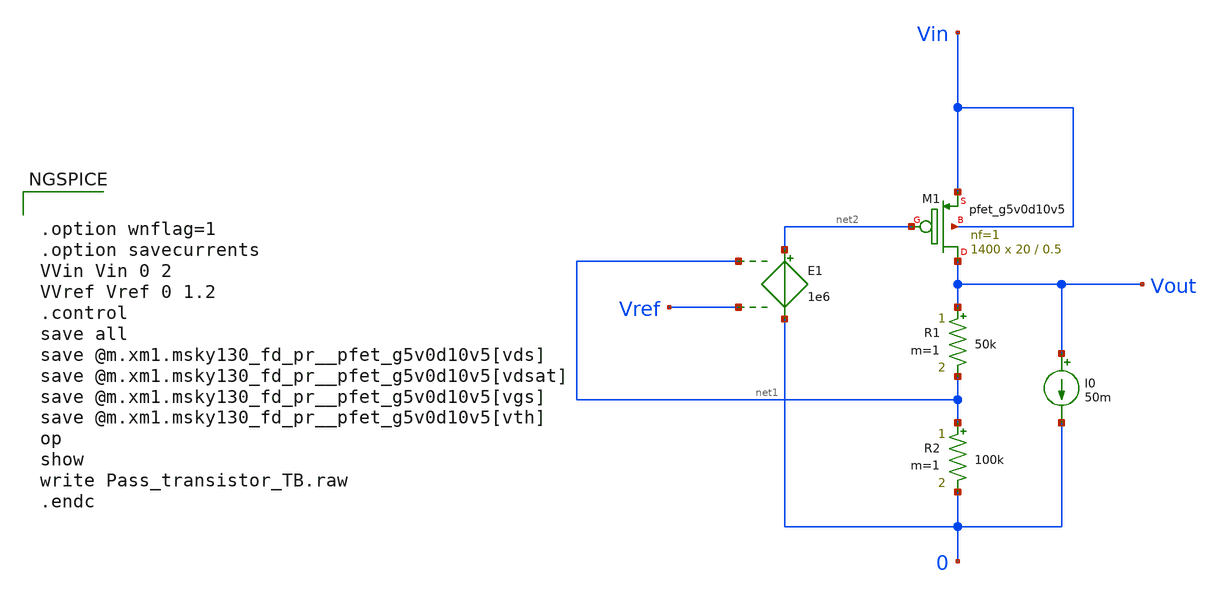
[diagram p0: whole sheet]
** sch_path: Analog_Blocks/LDO/Testbench/Pass_transistor_TB.sch
**.subckt Pass_transistor_TB
XM1 Vout net2 Vin Vin sky130_fd_pr__pfet_g5v0d10v5 L=0.5 W=20 nf=1 ad='int((nf+1)/2) * W/nf * 0.29' as='int((nf+2)/2) * W/nf * 0.29'
+ pd='2*int((nf+1)/2) * (W/nf + 0.29)' ps='2*int((nf+2)/2) * (W/nf + 0.29)' nrd='0.29 / W' nrs='0.29 / W'
+ sa=0 sb=0 sd=0 mult=1400 m=1400
R1 Vout net1 50k m=1
R2 net1 0 100k m=1
E1 net2 0 net1 Vref 1e6
I0 Vout 0 50m
**** begin user architecture code


.option wnflag=1
.option savecurrents
VVin Vin 0 2
VVref Vref 0 1.2
.control
save all
save @m.xm1.msky130_fd_pr__pfet_g5v0d10v5[vds]
save @m.xm1.msky130_fd_pr__pfet_g5v0d10v5[vdsat]
save @m.xm1.msky130_fd_pr__pfet_g5v0d10v5[vgs]
save @m.xm1.msky130_fd_pr__pfet_g5v0d10v5[vth]
op
show
write Pass_transistor_TB.raw
.endc




.param mc_mm_switch=0
.param mc_pr_switch=0
.include ~/mabrains/Analog_blocks/models/sky130A/libs.ref/sky130_fd_pr/spice/sky130_fd_pr__nfet_01v8__sf.corner.spice
.include ~/mabrains/Analog_blocks/models/sky130A/libs.ref/sky130_fd_pr/spice/sky130_fd_pr__nfet_01v8_lvt__sf.corner.spice
.include ~/mabrains/Analog_blocks/models/sky130A/libs.ref/sky130_fd_pr/spice/sky130_fd_pr__pfet_01v8__sf.corner.spice
.include ~/mabrains/Analog_blocks/models/sky130A/libs.ref/sky130_fd_pr/spice/sky130_fd_pr__nfet_03v3_nvt__sf.corner.spice
.include ~/mabrains/Analog_blocks/models/sky130A/libs.ref/sky130_fd_pr/spice/sky130_fd_pr__nfet_05v0_nvt__sf.corner.spice
.include ~/mabrains/Analog_blocks/models/sky130A/libs.ref/sky130_fd_pr/spice/sky130_fd_pr__esd_nfet_01v8__sf.corner.spice
.include ~/mabrains/Analog_blocks/models/sky130A/libs.ref/sky130_fd_pr/spice/sky130_fd_pr__pfet_01v8_lvt__sf.corner.spice
.include ~/mabrains/Analog_blocks/models/sky130A/libs.ref/sky130_fd_pr/spice/sky130_fd_pr__pfet_01v8_hvt__sf.corner.spice
.include ~/mabrains/Analog_blocks/models/sky130A/libs.ref/sky130_fd_pr/spice/sky130_fd_pr__esd_pfet_g5v0d10v5__sf.corner.spice
.include ~/mabrains/Analog_blocks/models/sky130A/libs.ref/sky130_fd_pr/spice/sky130_fd_pr__pfet_g5v0d10v5__sf.corner.spice
.include ~/mabrains/Analog_blocks/models/sky130A/libs.ref/sky130_fd_pr/spice/sky130_fd_pr__pfet_g5v0d16v0__sf.corner.spice
.include ~/mabrains/Analog_blocks/models/sky130A/libs.ref/sky130_fd_pr/spice/sky130_fd_pr__nfet_g5v0d10v5__sf.corner.spice
.include ~/mabrains/Analog_blocks/models/sky130A/libs.ref/sky130_fd_pr/spice/sky130_fd_pr__nfet_g5v0d16v0__sf_discrete.corner.spice
.include ~/mabrains/Analog_blocks/models/sky130A/libs.ref/sky130_fd_pr/spice/sky130_fd_pr__esd_nfet_g5v0d10v5__sf.corner.spice
.include ~/mabrains/Analog_blocks/models/sky130A/libs.ref/sky130_fd_pr/spice/sky130_fd_pr__pfet_20v0__sf_discrete.corner.spice
.include ~/mabrains/Analog_blocks/models/sky130A/libs.ref/sky130_fd_pr/spice/sky130_fd_pr__nfet_20v0__sf_discrete.corner.spice
.include ~/mabrains/Analog_blocks/models/sky130A/libs.tech/ngspice/corners/sf/nonfet.spice
* Mismatch parameters
.include ~/mabrains/Analog_blocks/models/sky130A/libs.ref/sky130_fd_pr/spice/sky130_fd_pr__nfet_01v8__mismatch.corner.spice
.include ~/mabrains/Analog_blocks/models/sky130A/libs.ref/sky130_fd_pr/spice/sky130_fd_pr__pfet_01v8__mismatch.corner.spice
.include ~/mabrains/Analog_blocks/models/sky130A/libs.ref/sky130_fd_pr/spice/sky130_fd_pr__nfet_01v8_lvt__mismatch.corner.spice
.include ~/mabrains/Analog_blocks/models/sky130A/libs.ref/sky130_fd_pr/spice/sky130_fd_pr__pfet_01v8_lvt__mismatch.corner.spice
.include ~/mabrains/Analog_blocks/models/sky130A/libs.ref/sky130_fd_pr/spice/sky130_fd_pr__pfet_01v8_hvt__mismatch.corner.spice
.include ~/mabrains/Analog_blocks/models/sky130A/libs.ref/sky130_fd_pr/spice/sky130_fd_pr__nfet_g5v0d10v5__mismatch.corner.spice
.include ~/mabrains/Analog_blocks/models/sky130A/libs.ref/sky130_fd_pr/spice/sky130_fd_pr__pfet_g5v0d10v5__mismatch.corner.spice
.include ~/mabrains/Analog_blocks/models/sky130A/libs.ref/sky130_fd_pr/spice/sky130_fd_pr__nfet_05v0_nvt__mismatch.corner.spice
.include ~/mabrains/Analog_blocks/models/sky130A/libs.ref/sky130_fd_pr/spice/sky130_fd_pr__nfet_03v3_nvt__mismatch.corner.spice
* Resistor/Capacitor
.include ~/mabrains/Analog_blocks/models/sky130A/libs.tech/ngspice/r+c/res_typical__cap_typical.spice
.include ~/mabrains/Analog_blocks/models/sky130A/libs.tech/ngspice/r+c/res_typical__cap_typical__lin.spice
* Special cells
.include ~/mabrains/Analog_blocks/models/sky130A/libs.tech/ngspice/corners/sf/specialized_cells.spice
* All models
.include ~/mabrains/Analog_blocks/models/sky130A/libs.tech/ngspice/all.spice
* Corner
.include ~/mabrains/Analog_blocks/models/sky130A/libs.tech/ngspice/corners/sf/rf.spice



**** end user architecture code
**.ends
.end
